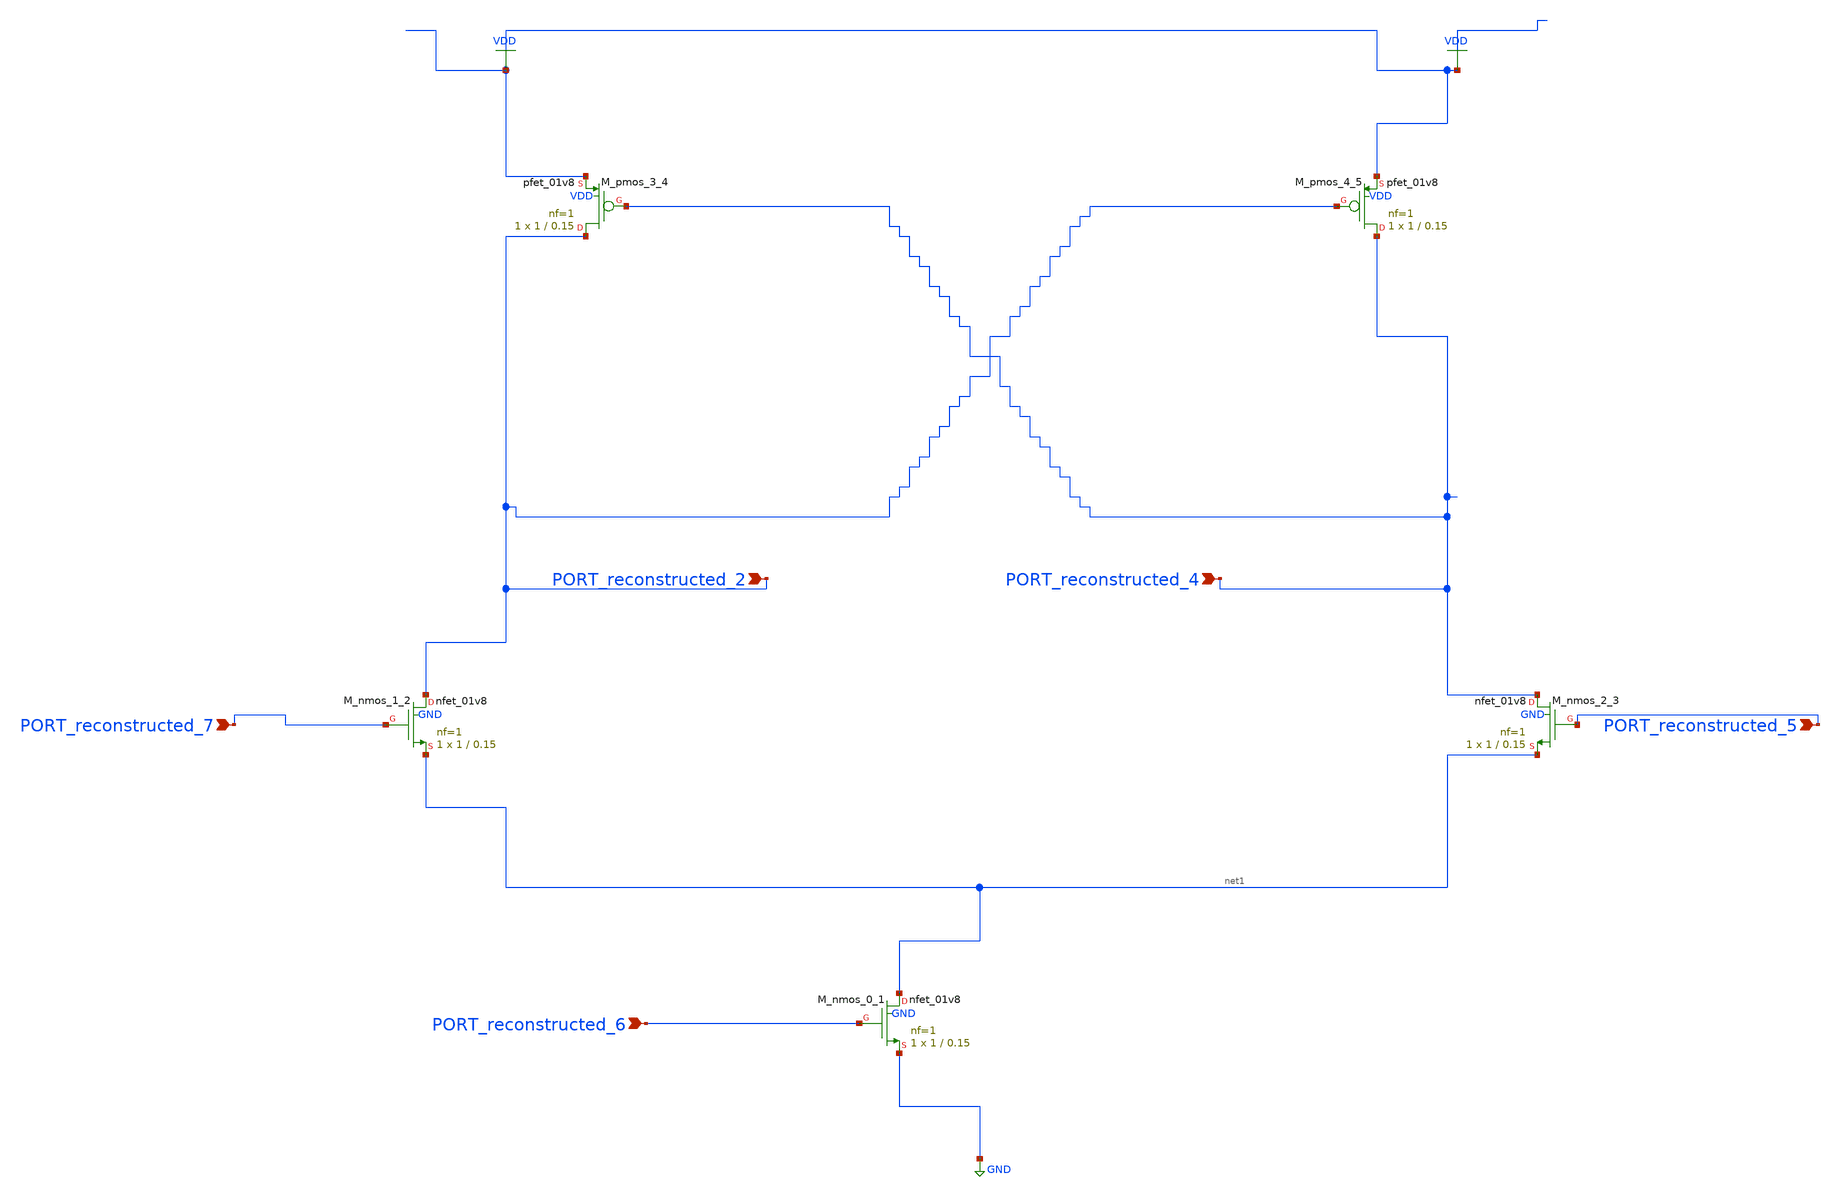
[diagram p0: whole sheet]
** sch_path: schematics/AMSNet/244.sch
**.subckt 244 PORT_reconstructed_5 PORT_reconstructed_6 PORT_reconstructed_4 PORT_reconstructed_2
*+ PORT_reconstructed_7
*.ipin PORT_reconstructed_5
*.ipin PORT_reconstructed_6
*.ipin PORT_reconstructed_4
*.ipin PORT_reconstructed_2
*.ipin PORT_reconstructed_7
XM_nmos_0_1 net1 PORT_reconstructed_6 GND GND sky130_fd_pr__nfet_01v8 L=0.15 W=1 nf=1 ad='int((1 + 1)/2) * 1 / 1 * 0.29'
+ as='int((1 + 2)/2) * 1 / 1 * 0.29' pd='2*int((1 + 1)/2) * (1 / 1 + 0.29)' ps='2*int((1 + 2)/2) * (1 / 1 + 0.29)'
+ nrd='0.29 / 1 ' nrs='0.29 / 1 ' sa=0 sb=0 sd=0 mult=1 m=1
XM_nmos_1_2 PORT_reconstructed_2 PORT_reconstructed_7 net1 GND sky130_fd_pr__nfet_01v8 L=0.15 W=1 nf=1
+ ad='int((1 + 1)/2) * 1 / 1 * 0.29' as='int((1 + 2)/2) * 1 / 1 * 0.29' pd='2*int((1 + 1)/2) * (1 / 1 + 0.29)'
+ ps='2*int((1 + 2)/2) * (1 / 1 + 0.29)' nrd='0.29 / 1 ' nrs='0.29 / 1 ' sa=0 sb=0 sd=0 mult=1 m=1
XM_nmos_2_3 PORT_reconstructed_4 PORT_reconstructed_5 net1 GND sky130_fd_pr__nfet_01v8 L=0.15 W=1 nf=1
+ ad='int((1 + 1)/2) * 1 / 1 * 0.29' as='int((1 + 2)/2) * 1 / 1 * 0.29' pd='2*int((1 + 1)/2) * (1 / 1 + 0.29)'
+ ps='2*int((1 + 2)/2) * (1 / 1 + 0.29)' nrd='0.29 / 1 ' nrs='0.29 / 1 ' sa=0 sb=0 sd=0 mult=1 m=1
XM_pmos_3_4 PORT_reconstructed_2 PORT_reconstructed_4 VDD VDD sky130_fd_pr__pfet_01v8 L=0.15 W=1 nf=1
+ ad='int((1 + 1)/2) * 1 / 1 * 0.29' as='int((1 + 2)/2) * 1 / 1 * 0.29' pd='2*int((1 + 1)/2) * (1 / 1 + 0.29)'
+ ps='2*int((1 + 2)/2) * (1 / 1 + 0.29)' nrd='0.29 / 1 ' nrs='0.29 / 1 ' sa=0 sb=0 sd=0 mult=1 m=1
XM_pmos_4_5 PORT_reconstructed_4 PORT_reconstructed_2 VDD VDD sky130_fd_pr__pfet_01v8 L=0.15 W=1 nf=1
+ ad='int((1 + 1)/2) * 1 / 1 * 0.29' as='int((1 + 2)/2) * 1 / 1 * 0.29' pd='2*int((1 + 1)/2) * (1 / 1 + 0.29)'
+ ps='2*int((1 + 2)/2) * (1 / 1 + 0.29)' nrd='0.29 / 1 ' nrs='0.29 / 1 ' sa=0 sb=0 sd=0 mult=1 m=1
**.ends
.GLOBAL GND
.GLOBAL VDD
.end
